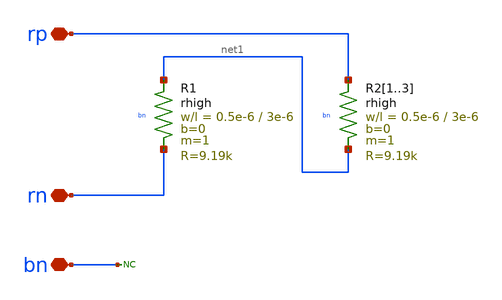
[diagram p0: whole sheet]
** sch_path: xschem/bandgap_banba_res-13k.sch
* (c) 2024-2025 H. Pretl, Apache-2.0 license
**.subckt bandgap_banba_res-13k rp rn bn
*.iopin rp
*.iopin rn
*.iopin bn
XR1 net1 rn bn rhigh w=0.5e-6 l=3e-6 m=1 b=0 mm_ok=1
XR21 rp net1 bn rhigh w=0.5e-6 l=3e-6 m=1 b=0 mm_ok=1
XR22 rp net1 bn rhigh w=0.5e-6 l=3e-6 m=1 b=0 mm_ok=1
XR23 rp net1 bn rhigh w=0.5e-6 l=3e-6 m=1 b=0 mm_ok=1
* noconn bn
**.ends
.end
